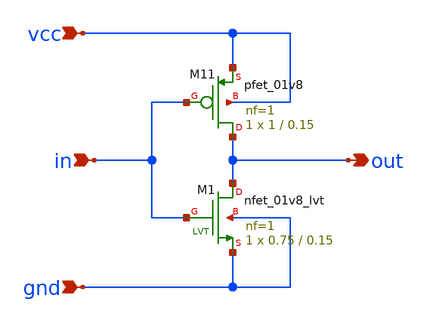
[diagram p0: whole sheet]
** sch_path: Oscillators/Ring-Oscillator/delay_cell.sch
**.subckt delay_cell vcc gnd in out
*.ipin vcc
*.ipin gnd
*.ipin in
*.opin out
XM1 out in gnd gnd sky130_fd_pr__nfet_01v8_lvt L=0.15 W=0.75 nf=1 ad='int((1 + 1)/2) * 0.75 / 1 * 0.29'
+ as='int((1 + 2)/2) * 0.75 / 1 * 0.29' pd='2*int((1 + 1)/2) * (0.75 / 1 + 0.29)' ps='2*int((1 + 2)/2) * (0.75 / 1 + 0.29)'
+ nrd='0.29 / 0.75 ' nrs='0.29 / 0.75 ' sa=0 sb=0 sd=0 mult=1 m=1
XM11 out in vcc vcc sky130_fd_pr__pfet_01v8 L=0.15 W=1 nf=1 ad='int((nf+1)/2) * W/nf * 0.29' as='int((nf+2)/2) * W/nf * 0.29'
+ pd='2*int((nf+1)/2) * (W/nf + 0.29)' ps='2*int((nf+2)/2) * (W/nf + 0.29)' nrd='0.29 / W' nrs='0.29 / W'
+ sa=0 sb=0 sd=0 mult=1 m=1
**.ends
.end
